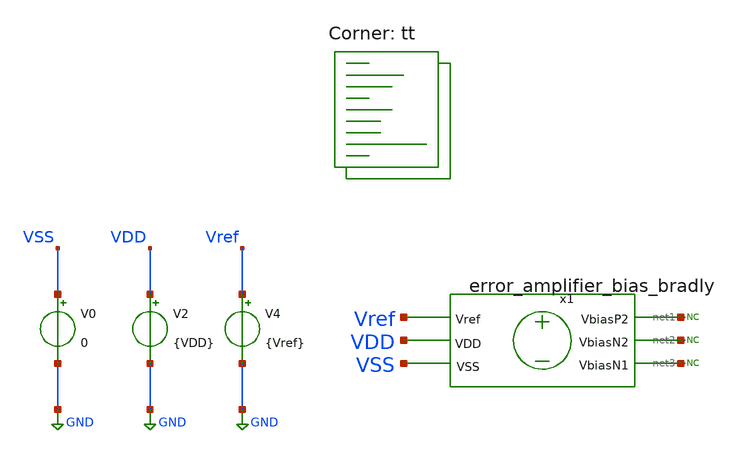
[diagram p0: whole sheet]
** sch_path: designs/used_and_to_delete/error_amplifier_bias_bradly/xschem/error_amplifier_bias_OP_130.sch
**.subckt error_amplifier_bias_OP_130
V0 VSS GND 0
V2 VDD GND {VDD}
V4 Vref GND {Vref}
* noconn #net1
* noconn #net2
* noconn #net3
x1 net3 net2 net1 VDD VSS Vref error_amplifier_bias_bradly
**** begin user architecture code
.lib $::SKYWATER_MODELS/sky130.lib.spice tt



.param VDD=1.8
.param Vref=1.2
.save

*nfet
  @m.x1.xm19.msky130_fd_pr__nfet_01v8[gm]  v(@m.x1.xm19.msky130_fd_pr__nfet_01v8[vth])
+  @m.x1.xm19.msky130_fd_pr__nfet_01v8[gds]  @m.x1.xm19.msky130_fd_pr__nfet_01v8[id]
  @m.x1.xm20.msky130_fd_pr__nfet_01v8[gm]  v(@m.x1.xm20.msky130_fd_pr__nfet_01v8[vth])
+  @m.x1.xm20.msky130_fd_pr__nfet_01v8[gds]  @m.x1.xm20.msky130_fd_pr__nfet_01v8[id]
  @m.x1.xm21.msky130_fd_pr__nfet_01v8[gm]  v(@m.x1.xm21.msky130_fd_pr__nfet_01v8[vth])
+  @m.x1.xm21.msky130_fd_pr__nfet_01v8[gds]  @m.x1.xm21.msky130_fd_pr__nfet_01v8[id]
  @m.x1.xm22.msky130_fd_pr__nfet_01v8[gm]  v(@m.x1.xm22.msky130_fd_pr__nfet_01v8[vth])
+  @m.x1.xm22.msky130_fd_pr__nfet_01v8[gds]  @m.x1.xm22.msky130_fd_pr__nfet_01v8[id]
  @m.x1.xm23.msky130_fd_pr__nfet_01v8[gm]  v(@m.x1.xm23.msky130_fd_pr__nfet_01v8[vth])
+  @m.x1.xm23.msky130_fd_pr__nfet_01v8[gds]  @m.x1.xm23.msky130_fd_pr__nfet_01v8[id]
  @m.x1.xm24.msky130_fd_pr__nfet_01v8[gm]  v(@m.x1.xm24.msky130_fd_pr__nfet_01v8[vth])
+  @m.x1.xm24.msky130_fd_pr__nfet_01v8[gds]  @m.x1.xm24.msky130_fd_pr__nfet_01v8[id]
  @m.x1.xm25.msky130_fd_pr__nfet_01v8[gm]  v(@m.x1.xm25.msky130_fd_pr__nfet_01v8[vth])
+  @m.x1.xm25.msky130_fd_pr__nfet_01v8[gds]  @m.x1.xm25.msky130_fd_pr__nfet_01v8[id]
  @m.x1.xm26.msky130_fd_pr__nfet_01v8[gm]  v(@m.x1.xm26.msky130_fd_pr__nfet_01v8[vth])
+  @m.x1.xm26.msky130_fd_pr__nfet_01v8[gds]  @m.x1.xm26.msky130_fd_pr__nfet_01v8[id]
  @m.x1.xm27.msky130_fd_pr__nfet_01v8[gm]  v(@m.x1.xm27.msky130_fd_pr__nfet_01v8[vth])
+  @m.x1.xm27.msky130_fd_pr__nfet_01v8[gds]  @m.x1.xm27.msky130_fd_pr__nfet_01v8[id]
  @m.x1.xm28.msky130_fd_pr__nfet_01v8[gm]  v(@m.x1.xm28.msky130_fd_pr__nfet_01v8[vth])
+  @m.x1.xm28.msky130_fd_pr__nfet_01v8[gds]  @m.x1.xm28.msky130_fd_pr__nfet_01v8[id]
  @m.x1.xm29.msky130_fd_pr__nfet_01v8[gm]  v(@m.x1.xm29.msky130_fd_pr__nfet_01v8[vth])
+  @m.x1.xm29.msky130_fd_pr__nfet_01v8[gds]  @m.x1.xm29.msky130_fd_pr__nfet_01v8[id]
  @m.x1.xm30.msky130_fd_pr__nfet_01v8[gm]  v(@m.x1.xm30.msky130_fd_pr__nfet_01v8[vth])
+  @m.x1.xm30.msky130_fd_pr__nfet_01v8[gds]  @m.x1.xm30.msky130_fd_pr__nfet_01v8[id]
  @m.x1.xm31.msky130_fd_pr__nfet_01v8[gm]  v(@m.x1.xm31.msky130_fd_pr__nfet_01v8[vth])
+  @m.x1.xm31.msky130_fd_pr__nfet_01v8[gds]  @m.x1.xm31.msky130_fd_pr__nfet_01v8[id]

*pfet
  @m.x1.xm12.msky130_fd_pr__pfet_01v8_lvt[gm]  v(@m.x1.xm12.msky130_fd_pr__pfet_01v8_lvt[vth])
+  @m.x1.xm12.msky130_fd_pr__pfet_01v8_lvt[gds]  @m.x1.xm12.msky130_fd_pr__pfet_01v8_lvt[id]
  @m.x1.xm13.msky130_fd_pr__pfet_01v8_lvt[gm]  v(@m.x1.xm13.msky130_fd_pr__pfet_01v8_lvt[vth])
+  @m.x1.xm13.msky130_fd_pr__pfet_01v8_lvt[gds]  @m.x1.xm13.msky130_fd_pr__pfet_01v8_lvt[id]
  @m.x1.xm14.msky130_fd_pr__pfet_01v8_lvt[gm]  v(@m.x1.xm14.msky130_fd_pr__pfet_01v8_lvt[vth])
+  @m.x1.xm14.msky130_fd_pr__pfet_01v8_lvt[gds]  @m.x1.xm14.msky130_fd_pr__pfet_01v8_lvt[id]
  @m.x1.xm15.msky130_fd_pr__pfet_01v8_lvt[gm]  v(@m.x1.xm15.msky130_fd_pr__pfet_01v8_lvt[vth])
+  @m.x1.xm15.msky130_fd_pr__pfet_01v8_lvt[gds]  @m.x1.xm15.msky130_fd_pr__pfet_01v8_lvt[id]
  @m.x1.xm16.msky130_fd_pr__pfet_01v8_lvt[gm]  v(@m.x1.xm16.msky130_fd_pr__pfet_01v8_lvt[vth])
+  @m.x1.xm16.msky130_fd_pr__pfet_01v8_lvt[gds]  @m.x1.xm16.msky130_fd_pr__pfet_01v8_lvt[id]
  @m.x1.xm17.msky130_fd_pr__pfet_01v8_lvt[gm]  v(@m.x1.xm17.msky130_fd_pr__pfet_01v8_lvt[vth])
+  @m.x1.xm17.msky130_fd_pr__pfet_01v8_lvt[gds]  @m.x1.xm17.msky130_fd_pr__pfet_01v8_lvt[id]
  @m.x1.xm18.msky130_fd_pr__pfet_01v8_lvt[gm]  v(@m.x1.xm18.msky130_fd_pr__pfet_01v8_lvt[vth])
+  @m.x1.xm18.msky130_fd_pr__pfet_01v8_lvt[gds]  @m.x1.xm18.msky130_fd_pr__pfet_01v8_lvt[id]

.control
  save all
  op
  write folded_cascode_bias_OP.raw
* Obtener voltajes en los nodos
let VbiasP2_voltage = v(net3)
let VbiasN2_voltage = v(net2)
let VbiasN1_voltage = v(net1)

* Imprimir voltajes en la consola
print VbiasP2_voltage VbiasN2_voltage VbiasN1_voltage

.endc



**** end user architecture code
**.ends

* expanding   symbol:
*+  /foss/designs/chipathon_2025/designs/sky130/error_amplifier_bias_bradly/xschem/error_amplifier_bias_bradly.sym # of pins=6
** sym_path: designs/used_and_to_delete/error_amplifier_bias_bradly/xschem/error_amplifier_bias_bradly.sym
** sch_path: designs/used_and_to_delete/error_amplifier_bias_bradly/xschem/error_amplifier_bias_bradly.sch
.subckt error_amplifier_bias_bradly VbiasN1 VbiasN2 VbiasP2 VDD VSS Vref
*.ipin Vref
*.iopin VbiasN1
*.iopin VbiasN2
*.iopin VDD
*.iopin VbiasP2
*.iopin VSS
XM19 vol vol VDD VDD pfet_03v3 L=2u W=0.26u nf=1 ad='int((nf+1)/2) * W/nf * 0.18u' as='int((nf+2)/2) * W/nf * 0.18u'
+ pd='2*int((nf+1)/2) * (W/nf + 0.18u)' ps='2*int((nf+2)/2) * (W/nf + 0.18u)' nrd='0.18u / W' nrs='0.18u / W'
+ sa=0 sb=0 sd=0 m=1
XM21 vol Vref v1 VSS nfet_03v3 L=2u W=1u nf=1 ad='int((nf+1)/2) * W/nf * 0.18u' as='int((nf+2)/2) * W/nf * 0.18u'
+ pd='2*int((nf+1)/2) * (W/nf + 0.18u)' ps='2*int((nf+2)/2) * (W/nf + 0.18u)' nrd='0.18u / W' nrs='0.18u / W'
+ sa=0 sb=0 sd=0 m=1
XM23 VbiasN2 vol VDD VDD pfet_03v3 L=2u W=0.26u nf=1 ad='int((nf+1)/2) * W/nf * 0.18u' as='int((nf+2)/2) * W/nf * 0.18u'
+ pd='2*int((nf+1)/2) * (W/nf + 0.18u)' ps='2*int((nf+2)/2) * (W/nf + 0.18u)' nrd='0.18u / W' nrs='0.18u / W'
+ sa=0 sb=0 sd=0 m=1
XM24 net1 VbiasN2 VSS VSS nfet_03v3 L=2u W=0.26u nf=1 ad='int((nf+1)/2) * W/nf * 0.18u' as='int((nf+2)/2) * W/nf * 0.18u'
+ pd='2*int((nf+1)/2) * (W/nf + 0.18u)' ps='2*int((nf+2)/2) * (W/nf + 0.18u)' nrd='0.18u / W' nrs='0.18u / W'
+ sa=0 sb=0 sd=0 m=1
XM25 v1 Vref v2 VSS nfet_03v3 L=2u W=1u nf=1 ad='int((nf+1)/2) * W/nf * 0.18u' as='int((nf+2)/2) * W/nf * 0.18u'
+ pd='2*int((nf+1)/2) * (W/nf + 0.18u)' ps='2*int((nf+2)/2) * (W/nf + 0.18u)' nrd='0.18u / W' nrs='0.18u / W'
+ sa=0 sb=0 sd=0 m=1
XM26 v2 Vref VSS VSS nfet_03v3 L=2u W=1u nf=1 ad='int((nf+1)/2) * W/nf * 0.18u' as='int((nf+2)/2) * W/nf * 0.18u'
+ pd='2*int((nf+1)/2) * (W/nf + 0.18u)' ps='2*int((nf+2)/2) * (W/nf + 0.18u)' nrd='0.18u / W' nrs='0.18u / W'
+ sa=0 sb=0 sd=0 m=1
XM27 net2 VbiasN2 net1 VSS nfet_03v3 L=2u W=0.26u nf=1 ad='int((nf+1)/2) * W/nf * 0.18u' as='int((nf+2)/2) * W/nf * 0.18u'
+ pd='2*int((nf+1)/2) * (W/nf + 0.18u)' ps='2*int((nf+2)/2) * (W/nf + 0.18u)' nrd='0.18u / W' nrs='0.18u / W'
+ sa=0 sb=0 sd=0 m=1
XM28 VbiasN2 VbiasN2 net2 VSS nfet_03v3 L=2u W=0.26u nf=1 ad='int((nf+1)/2) * W/nf * 0.18u' as='int((nf+2)/2) * W/nf * 0.18u'
+ pd='2*int((nf+1)/2) * (W/nf + 0.18u)' ps='2*int((nf+2)/2) * (W/nf + 0.18u)' nrd='0.18u / W' nrs='0.18u / W'
+ sa=0 sb=0 sd=0 m=1
XM29 VbiasN1 vol VDD VDD pfet_03v3 L=2u W=0.24u nf=1 ad='int((nf+1)/2) * W/nf * 0.18u' as='int((nf+2)/2) * W/nf * 0.18u'
+ pd='2*int((nf+1)/2) * (W/nf + 0.18u)' ps='2*int((nf+2)/2) * (W/nf + 0.18u)' nrd='0.18u / W' nrs='0.18u / W'
+ sa=0 sb=0 sd=0 m=1
XM30 Vbb VbiasN1 VSS VSS nfet_03v3 L=2u W=1.8u nf=1 ad='int((nf+1)/2) * W/nf * 0.18u' as='int((nf+2)/2) * W/nf * 0.18u'
+ pd='2*int((nf+1)/2) * (W/nf + 0.18u)' ps='2*int((nf+2)/2) * (W/nf + 0.18u)' nrd='0.18u / W' nrs='0.18u / W'
+ sa=0 sb=0 sd=0 m=1
XM31 VbiasN1 VbiasN2 net3 VSS nfet_03v3 L=2u W=0.3u nf=1 ad='int((nf+1)/2) * W/nf * 0.18u' as='int((nf+2)/2) * W/nf * 0.18u'
+ pd='2*int((nf+1)/2) * (W/nf + 0.18u)' ps='2*int((nf+2)/2) * (W/nf + 0.18u)' nrd='0.18u / W' nrs='0.18u / W'
+ sa=0 sb=0 sd=0 m=1
XM32 net3 VbiasN2 Vbb VSS nfet_03v3 L=2u W=0.3u nf=1 ad='int((nf+1)/2) * W/nf * 0.18u' as='int((nf+2)/2) * W/nf * 0.18u'
+ pd='2*int((nf+1)/2) * (W/nf + 0.18u)' ps='2*int((nf+2)/2) * (W/nf + 0.18u)' nrd='0.18u / W' nrs='0.18u / W'
+ sa=0 sb=0 sd=0 m=1
XM333 VbiasP2 VbiasN2 net4 VSS nfet_03v3 L=2u W=1u nf=1 ad='int((nf+1)/2) * W/nf * 0.18u' as='int((nf+2)/2) * W/nf * 0.18u'
+ pd='2*int((nf+1)/2) * (W/nf + 0.18u)' ps='2*int((nf+2)/2) * (W/nf + 0.18u)' nrd='0.18u / W' nrs='0.18u / W'
+ sa=0 sb=0 sd=0 m=1
XM34 net4 VbiasN1 VSS VSS nfet_03v3 L=2u W=1.5u nf=1 ad='int((nf+1)/2) * W/nf * 0.18u' as='int((nf+2)/2) * W/nf * 0.18u'
+ pd='2*int((nf+1)/2) * (W/nf + 0.18u)' ps='2*int((nf+2)/2) * (W/nf + 0.18u)' nrd='0.18u / W' nrs='0.18u / W'
+ sa=0 sb=0 sd=0 m=1
XM35 net5 VbiasP2 VDD VDD pfet_03v3 L=2u W=1.3u nf=1 ad='int((nf+1)/2) * W/nf * 0.18u' as='int((nf+2)/2) * W/nf * 0.18u'
+ pd='2*int((nf+1)/2) * (W/nf + 0.18u)' ps='2*int((nf+2)/2) * (W/nf + 0.18u)' nrd='0.18u / W' nrs='0.18u / W'
+ sa=0 sb=0 sd=0 m=1
XM36 net6 VbiasP2 net5 VDD pfet_03v3 L=2u W=1.3u nf=1 ad='int((nf+1)/2) * W/nf * 0.18u' as='int((nf+2)/2) * W/nf * 0.18u'
+ pd='2*int((nf+1)/2) * (W/nf + 0.18u)' ps='2*int((nf+2)/2) * (W/nf + 0.18u)' nrd='0.18u / W' nrs='0.18u / W'
+ sa=0 sb=0 sd=0 m=1
XM37 VbiasP2 VbiasP2 net6 VDD pfet_03v3 L=2u W=1.3u nf=1 ad='int((nf+1)/2) * W/nf * 0.18u' as='int((nf+2)/2) * W/nf * 0.18u'
+ pd='2*int((nf+1)/2) * (W/nf + 0.18u)' ps='2*int((nf+2)/2) * (W/nf + 0.18u)' nrd='0.18u / W' nrs='0.18u / W'
+ sa=0 sb=0 sd=0 m=1
.ends

.GLOBAL GND
.end
